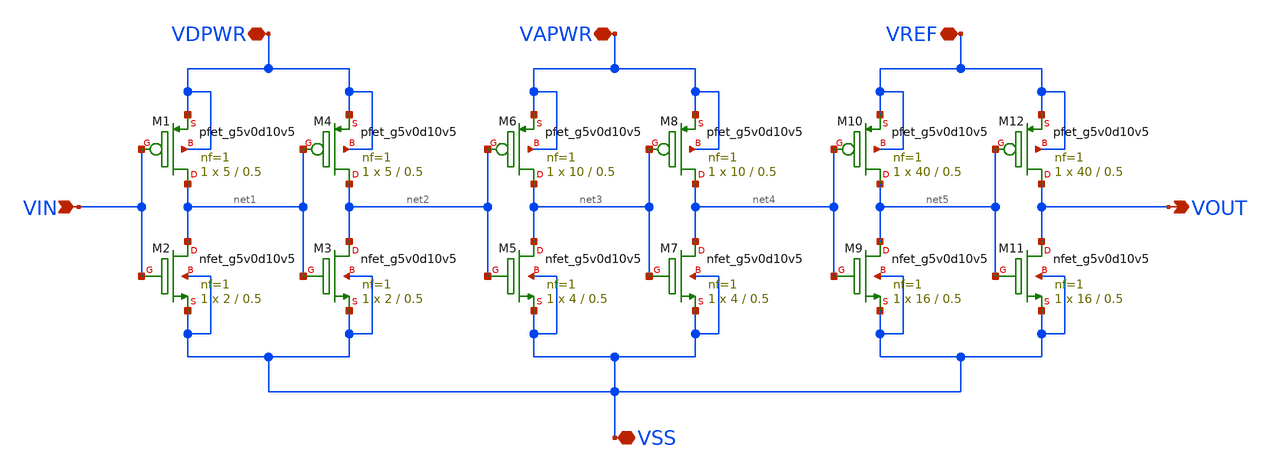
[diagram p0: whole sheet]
** sch_path: SKY130/SAR-ADC/SAR-ADC_5.0V/LV_SHIF_D2A.sch
**.subckt LV_SHIF_D2A VDPWR VSS VAPWR VREF VIN VOUT
*.iopin VDPWR
*.iopin VSS
*.iopin VAPWR
*.iopin VREF
*.ipin VIN
*.opin VOUT
XM2 net1 VIN VSS VSS sky130_fd_pr__nfet_g5v0d10v5 L=0.5 W=2 nf=1 ad='int((1 + 1)/2) * 2 / 1 * 0.29' as='int((1 + 2)/2) * 2 / 1 * 0.29'
+ pd='2*int((1 + 1)/2) * (2 / 1 + 0.29)' ps='2*int((1 + 2)/2) * (2 / 1 + 0.29)' nrd='0.29 / 2 ' nrs='0.29 / 2 '
+ sa=0 sb=0 sd=0 mult=1 m=1
XM1 net1 VIN VDPWR VDPWR sky130_fd_pr__pfet_g5v0d10v5 L=0.5 W=5 nf=1 ad='int((1 + 1)/2) * 5 / 1 * 0.29'
+ as='int((1 + 2)/2) * 5 / 1 * 0.29' pd='2*int((1 + 1)/2) * (5 / 1 + 0.29)' ps='2*int((1 + 2)/2) * (5 / 1 + 0.29)'
+ nrd='0.29 / 5 ' nrs='0.29 / 5 ' sa=0 sb=0 sd=0 mult=1 m=1
XM3 net2 net1 VSS VSS sky130_fd_pr__nfet_g5v0d10v5 L=0.5 W=2 nf=1 ad='int((1 + 1)/2) * 2 / 1 * 0.29'
+ as='int((1 + 2)/2) * 2 / 1 * 0.29' pd='2*int((1 + 1)/2) * (2 / 1 + 0.29)' ps='2*int((1 + 2)/2) * (2 / 1 + 0.29)'
+ nrd='0.29 / 2 ' nrs='0.29 / 2 ' sa=0 sb=0 sd=0 mult=1 m=1
XM4 net2 net1 VDPWR VDPWR sky130_fd_pr__pfet_g5v0d10v5 L=0.5 W=5 nf=1 ad='int((1 + 1)/2) * 5 / 1 * 0.29'
+ as='int((1 + 2)/2) * 5 / 1 * 0.29' pd='2*int((1 + 1)/2) * (5 / 1 + 0.29)' ps='2*int((1 + 2)/2) * (5 / 1 + 0.29)'
+ nrd='0.29 / 5 ' nrs='0.29 / 5 ' sa=0 sb=0 sd=0 mult=1 m=1
XM5 net3 net2 VSS VSS sky130_fd_pr__nfet_g5v0d10v5 L=0.5 W=4 nf=1 ad='int((1 + 1)/2) * 4 / 1 * 0.29'
+ as='int((1 + 2)/2) * 4 / 1 * 0.29' pd='2*int((1 + 1)/2) * (4 / 1 + 0.29)' ps='2*int((1 + 2)/2) * (4 / 1 + 0.29)'
+ nrd='0.29 / 4 ' nrs='0.29 / 4 ' sa=0 sb=0 sd=0 mult=1 m=1
XM6 net3 net2 VAPWR VAPWR sky130_fd_pr__pfet_g5v0d10v5 L=0.5 W=10 nf=1 ad='int((1 + 1)/2) * 10 / 1 * 0.29'
+ as='int((1 + 2)/2) * 10 / 1 * 0.29' pd='2*int((1 + 1)/2) * (10 / 1 + 0.29)' ps='2*int((1 + 2)/2) * (10 / 1 + 0.29)'
+ nrd='0.29 / 10 ' nrs='0.29 / 10 ' sa=0 sb=0 sd=0 mult=1 m=1
XM7 net4 net3 VSS VSS sky130_fd_pr__nfet_g5v0d10v5 L=0.5 W=4 nf=1 ad='int((1 + 1)/2) * 4 / 1 * 0.29'
+ as='int((1 + 2)/2) * 4 / 1 * 0.29' pd='2*int((1 + 1)/2) * (4 / 1 + 0.29)' ps='2*int((1 + 2)/2) * (4 / 1 + 0.29)'
+ nrd='0.29 / 4 ' nrs='0.29 / 4 ' sa=0 sb=0 sd=0 mult=1 m=1
XM8 net4 net3 VAPWR VAPWR sky130_fd_pr__pfet_g5v0d10v5 L=0.5 W=10 nf=1 ad='int((1 + 1)/2) * 10 / 1 * 0.29'
+ as='int((1 + 2)/2) * 10 / 1 * 0.29' pd='2*int((1 + 1)/2) * (10 / 1 + 0.29)' ps='2*int((1 + 2)/2) * (10 / 1 + 0.29)'
+ nrd='0.29 / 10 ' nrs='0.29 / 10 ' sa=0 sb=0 sd=0 mult=1 m=1
XM9 net5 net4 VSS VSS sky130_fd_pr__nfet_g5v0d10v5 L=0.5 W=16 nf=1 ad='int((1 + 1)/2) * 16 / 1 * 0.29'
+ as='int((1 + 2)/2) * 16 / 1 * 0.29' pd='2*int((1 + 1)/2) * (16 / 1 + 0.29)' ps='2*int((1 + 2)/2) * (16 / 1 + 0.29)'
+ nrd='0.29 / 16 ' nrs='0.29 / 16 ' sa=0 sb=0 sd=0 mult=1 m=1
XM10 net5 net4 VREF VREF sky130_fd_pr__pfet_g5v0d10v5 L=0.5 W=40 nf=1 ad='int((1 + 1)/2) * 40 / 1 * 0.29'
+ as='int((1 + 2)/2) * 40 / 1 * 0.29' pd='2*int((1 + 1)/2) * (40 / 1 + 0.29)' ps='2*int((1 + 2)/2) * (40 / 1 + 0.29)'
+ nrd='0.29 / 40 ' nrs='0.29 / 40 ' sa=0 sb=0 sd=0 mult=1 m=1
XM11 VOUT net5 VSS VSS sky130_fd_pr__nfet_g5v0d10v5 L=0.5 W=16 nf=1 ad='int((1 + 1)/2) * 16 / 1 * 0.29'
+ as='int((1 + 2)/2) * 16 / 1 * 0.29' pd='2*int((1 + 1)/2) * (16 / 1 + 0.29)' ps='2*int((1 + 2)/2) * (16 / 1 + 0.29)'
+ nrd='0.29 / 16 ' nrs='0.29 / 16 ' sa=0 sb=0 sd=0 mult=1 m=1
XM12 VOUT net5 VREF VREF sky130_fd_pr__pfet_g5v0d10v5 L=0.5 W=40 nf=1 ad='int((1 + 1)/2) * 40 / 1 * 0.29'
+ as='int((1 + 2)/2) * 40 / 1 * 0.29' pd='2*int((1 + 1)/2) * (40 / 1 + 0.29)' ps='2*int((1 + 2)/2) * (40 / 1 + 0.29)'
+ nrd='0.29 / 40 ' nrs='0.29 / 40 ' sa=0 sb=0 sd=0 mult=1 m=1
**.ends
.end
